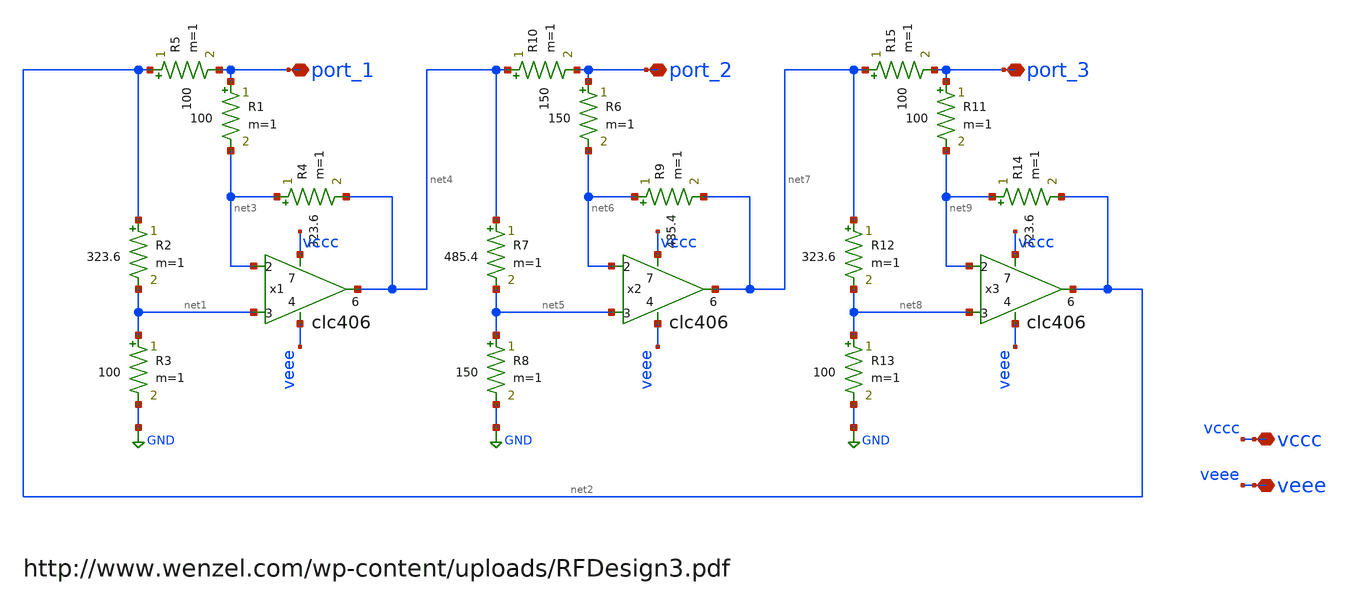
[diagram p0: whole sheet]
** sch_path: circulator/active_circulator.sch
**.subckt active_circulator port_1 port_2 port_3 vccc veee
*.iopin port_1
*.iopin port_2
*.iopin port_3
*.iopin vccc
*.iopin veee
R1 port_1 net3 100 m=1
R2 net2 net1 323.6 m=1
R3 net1 GND 100 m=1
R4 net3 net4 323.6 m=1
R5 net2 port_1 100 m=1
R6 port_2 net6 150 m=1
R7 net4 net5 485.4 m=1
R8 net5 GND 150 m=1
R9 net6 net7 485.4 m=1
R10 net4 port_2 150 m=1
R11 port_3 net9 100 m=1
R12 net7 net8 323.6 m=1
R13 net8 GND 100 m=1
R14 net9 net2 323.6 m=1
R15 net7 port_3 100 m=1
x1 net1 net3 net4 vccc veee clc406
x2 net5 net6 net7 vccc veee clc406
x3 net8 net9 net2 vccc veee clc406
**.ends
.GLOBAL GND
.end
